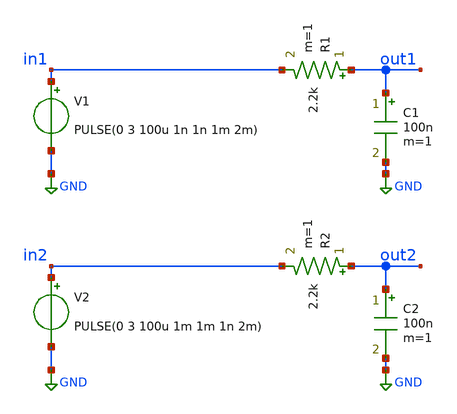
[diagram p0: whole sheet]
** sch_path: examples/analog_rc/circuit.sch
**.subckt circuit
V1 in1 GND PULSE(0 3 100u 1n 1n 1m 2m)
V2 in2 GND PULSE(0 3 100u 1m 1m 1n 2m)
R1 out1 in1 2.2k m=1
R2 out2 in2 2.2k m=1
C1 out1 GND 100n m=1
C2 out2 GND 100n m=1
**** begin user architecture code


.control
  tran 100n 10m
  plot v(in1) v(out1)
  plot v(in2) v(out2)
.endc


**** end user architecture code
**.ends
.GLOBAL GND
.end
